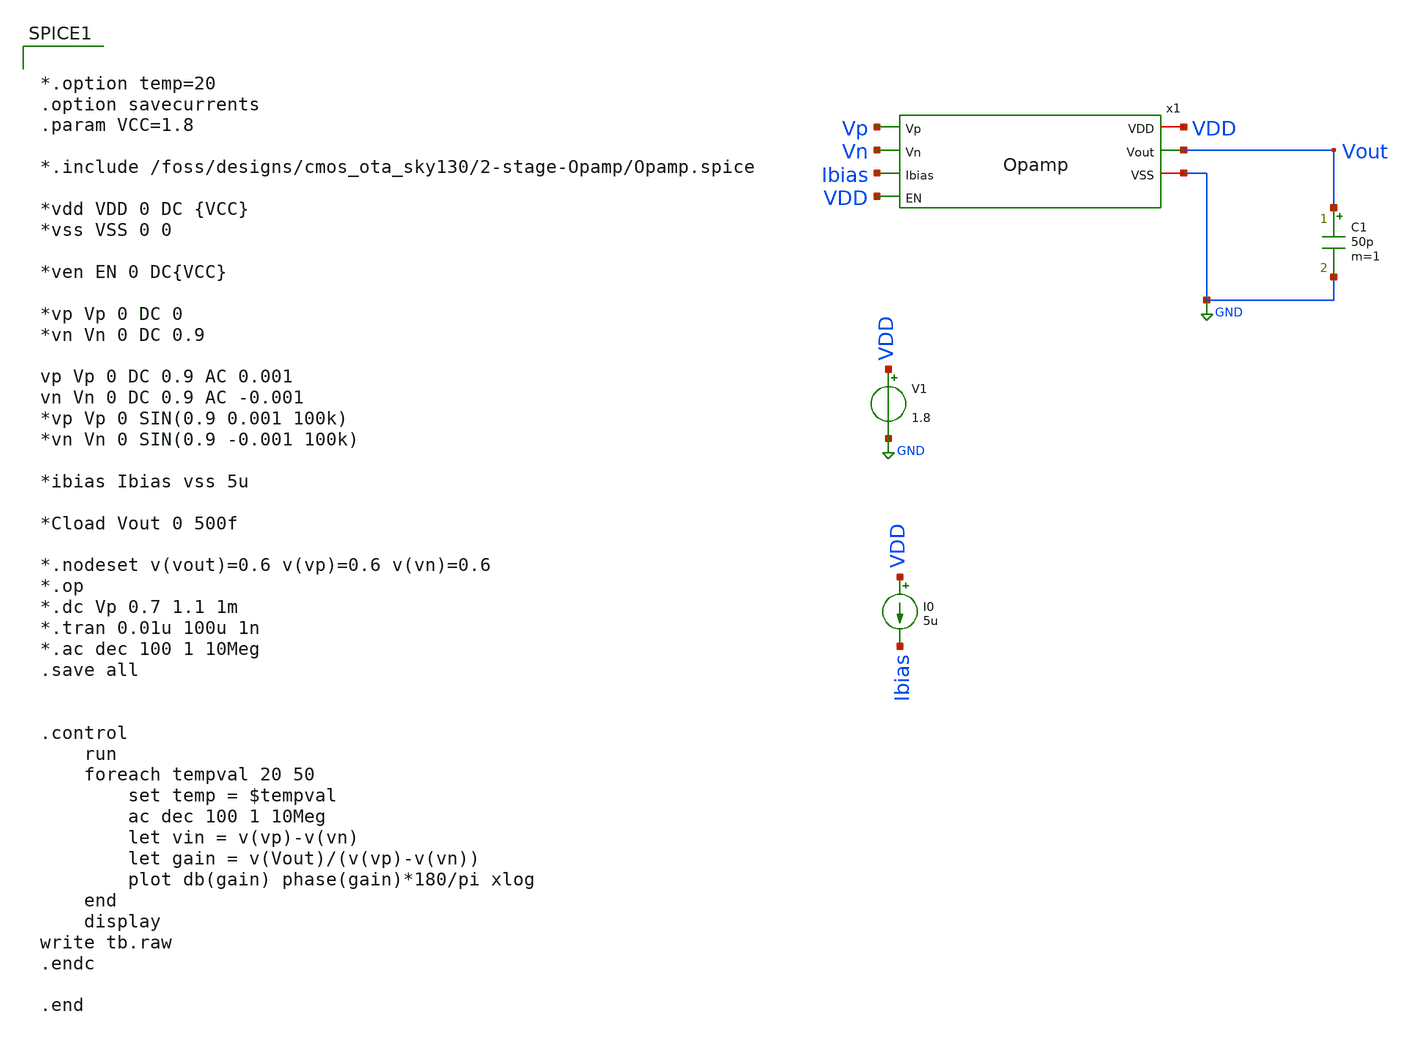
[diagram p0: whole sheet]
** sch_path: xschem/tb_Opamp.sch
**.subckt tb_Opamp
V1 VDD GND 1.8
C1 Vout GND 50p m=1
I0 VDD Ibias 5u
x1 VDD Vp Vn Vout Ibias GND VDD Opamp
**** begin user architecture code

** opencircuitdesign pdks install
.lib /foss/pdks/sky130A/libs.tech/ngspice/sky130.lib.spice tt




*.option temp=20
.option savecurrents
.param VCC=1.8

*.include /foss/designs/cmos_ota_sky130/2-stage-Opamp/Opamp.spice

*vdd VDD 0 DC {VCC}
*vss VSS 0 0

*ven EN 0 DC{VCC}

*vp Vp 0 DC 0
*vn Vn 0 DC 0.9

vp Vp 0 DC 0.9 AC 0.001
vn Vn 0 DC 0.9 AC -0.001
*vp Vp 0 SIN(0.9 0.001 100k)
*vn Vn 0 SIN(0.9 -0.001 100k)

*ibias Ibias vss 5u

*Cload Vout 0 500f

*.nodeset v(vout)=0.6 v(vp)=0.6 v(vn)=0.6
*.op
*.dc Vp 0.7 1.1 1m
*.tran 0.01u 100u 1n
*.ac dec 100 1 10Meg
.save all


.control
	run
	foreach tempval 20 50
		set temp = $tempval
		ac dec 100 1 10Meg
		let vin = v(vp)-v(vn)
		let gain = v(Vout)/(v(vp)-v(vn))
		plot db(gain) phase(gain)*180/pi xlog
	end
	display
write tb.raw
.endc

.end


**** end user architecture code
**.ends

* expanding   symbol:  /foss/designs/ttsky_se_opamp/xschem/Opamp.sym # of pins=7
** sym_path: xschem/Opamp.sym
** sch_path: xschem/Opamp.sch
.subckt Opamp VDD Vp Vn Vout Ibias VSS EN
*.ipin Vn
*.ipin Ibias
*.ipin Vp
*.ipin EN
*.opin Vout
*.iopin VSS
*.iopin VDD
XM2 Vouts1 Vp Itail GND sky130_fd_pr__nfet_01v8 L=1 W=4 nf=2 ad='int((nf+1)/2) * W/nf * 0.29' as='int((nf+2)/2) * W/nf * 0.29'
+ pd='2*int((nf+1)/2) * (W/nf + 0.29)' ps='2*int((nf+2)/2) * (W/nf + 0.29)' nrd='0.29 / W' nrs='0.29 / W'
+ sa=0 sb=0 sd=0 mult=1 m=1
XM4 Vouts1 net1 VDD VDD sky130_fd_pr__pfet_01v8 L=1 W=4 nf=2 ad='int((nf+1)/2) * W/nf * 0.29' as='int((nf+2)/2) * W/nf * 0.29'
+ pd='2*int((nf+1)/2) * (W/nf + 0.29)' ps='2*int((nf+2)/2) * (W/nf + 0.29)' nrd='0.29 / W' nrs='0.29 / W'
+ sa=0 sb=0 sd=0 mult=2 m=2
XM3 net1 net1 VDD VDD sky130_fd_pr__pfet_01v8 L=1 W=4 nf=2 ad='int((nf+1)/2) * W/nf * 0.29' as='int((nf+2)/2) * W/nf * 0.29'
+ pd='2*int((nf+1)/2) * (W/nf + 0.29)' ps='2*int((nf+2)/2) * (W/nf + 0.29)' nrd='0.29 / W' nrs='0.29 / W'
+ sa=0 sb=0 sd=0 mult=2 m=2
XM1 net1 Vn Itail GND sky130_fd_pr__nfet_01v8 L=1 W=4 nf=2 ad='int((nf+1)/2) * W/nf * 0.29' as='int((nf+2)/2) * W/nf * 0.29'
+ pd='2*int((nf+1)/2) * (W/nf + 0.29)' ps='2*int((nf+2)/2) * (W/nf + 0.29)' nrd='0.29 / W' nrs='0.29 / W'
+ sa=0 sb=0 sd=0 mult=1 m=1
XM6 Vout Vouts1 VDD VDD sky130_fd_pr__pfet_01v8 L=1 W=7.5 nf=4 ad='int((nf+1)/2) * W/nf * 0.29' as='int((nf+2)/2) * W/nf * 0.29'
+ pd='2*int((nf+1)/2) * (W/nf + 0.29)' ps='2*int((nf+2)/2) * (W/nf + 0.29)' nrd='0.29 / W' nrs='0.29 / W'
+ sa=0 sb=0 sd=0 mult=3 m=3
XM5 Itail Ibias VSS VSS sky130_fd_pr__nfet_01v8 L=1 W=4 nf=4 ad='int((nf+1)/2) * W/nf * 0.29' as='int((nf+2)/2) * W/nf * 0.29'
+ pd='2*int((nf+1)/2) * (W/nf + 0.29)' ps='2*int((nf+2)/2) * (W/nf + 0.29)' nrd='0.29 / W' nrs='0.29 / W'
+ sa=0 sb=0 sd=0 mult=5 m=5
XM7 Vout Ibias VSS VSS sky130_fd_pr__nfet_01v8 L=1 W=4 nf=4 ad='int((nf+1)/2) * W/nf * 0.29' as='int((nf+2)/2) * W/nf * 0.29'
+ pd='2*int((nf+1)/2) * (W/nf + 0.29)' ps='2*int((nf+2)/2) * (W/nf + 0.29)' nrd='0.29 / W' nrs='0.29 / W'
+ sa=0 sb=0 sd=0 mult=6 m=6
XM8 Ibias Ibias VSS VSS sky130_fd_pr__nfet_01v8 L=1 W=4 nf=4 ad='int((nf+1)/2) * W/nf * 0.29' as='int((nf+2)/2) * W/nf * 0.29'
+ pd='2*int((nf+1)/2) * (W/nf + 0.29)' ps='2*int((nf+2)/2) * (W/nf + 0.29)' nrd='0.29 / W' nrs='0.29 / W'
+ sa=0 sb=0 sd=0 mult=1 m=1
XM9 VSS EN Ibias Ibias sky130_fd_pr__pfet_01v8 L=1 W=4 nf=1 ad='int((nf+1)/2) * W/nf * 0.29' as='int((nf+2)/2) * W/nf * 0.29'
+ pd='2*int((nf+1)/2) * (W/nf + 0.29)' ps='2*int((nf+2)/2) * (W/nf + 0.29)' nrd='0.29 / W' nrs='0.29 / W'
+ sa=0 sb=0 sd=0 mult=1 m=1
XM10 VSS EN Ibias Ibias sky130_fd_pr__pfet_01v8 L=1 W=4 nf=1 ad='int((nf+1)/2) * W/nf * 0.29' as='int((nf+2)/2) * W/nf * 0.29'
+ pd='2*int((nf+1)/2) * (W/nf + 0.29)' ps='2*int((nf+2)/2) * (W/nf + 0.29)' nrd='0.29 / W' nrs='0.29 / W'
+ sa=0 sb=0 sd=0 mult=1 m=1
XC2 net2 Vout sky130_fd_pr__cap_mim_m3_1 W=30 L=75 MF=2 m=2
Rz net2 Vouts1 sky130_fd_pr__res_generic_l1 W=0.04 L=50 m=1
**** begin user architecture code
"Is Subcircuit" = YES
**** end user architecture code
.ends

.GLOBAL GND
.end
